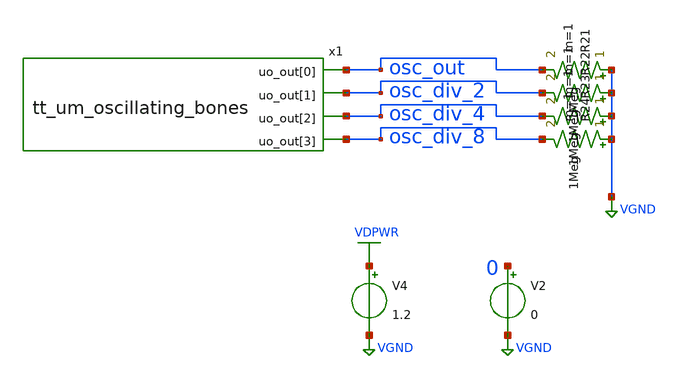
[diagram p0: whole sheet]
** sch_path: xschem/testbench.sch
**.subckt testbench
x1 osc_out osc_div_2 osc_div_4 osc_div_8 tt_um_oscillating_bones
R21 VGND osc_out 1Meg m=1
R22 VGND osc_div_2 1Meg m=1
R23 VGND osc_div_4 1Meg m=1
R24 VGND osc_div_8 1Meg m=1
V2 0 VGND 0
V4 VDPWR VGND 1.2
**** begin user architecture code

.lib $::SG13G2_MODELS/cornerMOSlv.lib mos_tt
.include ${PDK_ROOT}/${PDK}/libs.ref/sg13g2_stdcell/spice/sg13g2_stdcell.spice



.param temp=27
.param mc_ok=1

.tran 50p 200n
.save all

.control
run

meas tran tdiff TRIG osc_out VAL=1.1 RISE=2 TARG osc_out VAL=1.1 RISE=3
let osc_freq_mhz = (1 / (tdiff) / 1e6)
save osc_freq_mhz

meas tran tdiff_div2 TRIG osc_div_2 VAL=1.1 RISE=2 TARG osc_div_2 VAL=1.1 RISE=3
let osc_div_2_freq_mhz = (1 / (tdiff_div2) / 1e6)
save osc_div_2_freq_mhz

meas tran tdiff_div4 TRIG osc_div_4 VAL=1.1 RISE=2 TARG osc_div_4 VAL=1.1 RISE=3
let osc_div_4_freq_mhz = (1 / (tdiff_div4) / 1e6)
save osc_div_4_freq_mhz

meas tran tdiff_div8 TRIG osc_div_8 VAL=1.1 RISE=2 TARG osc_div_8 VAL=1.1 RISE=3
let osc_div_8_freq_mhz = (1 / (tdiff_div8) / 1e6)
save osc_div_8_freq_mhz

write testbench.raw
.endc


**** end user architecture code
**.ends

* expanding   symbol:  tt_um_oscillating_bones.sym # of pins=4
** sym_path: xschem/tt_um_oscillating_bones.sym
** sch_path: xschem/tt_um_oscillating_bones.sch
.subckt tt_um_oscillating_bones uo_out[0] uo_out[1] uo_out[2] uo_out[3]
*.opin uo_out[1]
*.opin uo_out[0]
*.opin uo_out[2]
*.opin uo_out[3]
x22 uo_out[1] uo_out[2] uo_out[3] uo_out[0] freq_divider
x1 uo_out[0] ring
.ends


* expanding   symbol:  freq_divider.sym # of pins=4
** sym_path: xschem/freq_divider.sym
** sch_path: xschem/freq_divider.sch
.subckt freq_divider ODIV2 ODIV4 ODIV8 IN
*.ipin IN
*.opin ODIV2
*.opin ODIV4
*.opin ODIV8
x4 ODIV2 net3 IN net3 VDPWR VDD VSS sg13g2_dfrbp_2
x1 ODIV4 net1 ODIV2 net1 VDPWR VDD VSS sg13g2_dfrbp_2
x2 ODIV8 net2 ODIV4 net2 VDPWR VDD VSS sg13g2_dfrbp_2
.ends


* expanding   symbol:  ring.sym # of pins=1
** sym_path: xschem/ring.sym
** sch_path: xschem/ring.sch
.subckt ring ROSC_OUT
*.opin ROSC_OUT
x1 net20 net1 skullfet_inverter
x2 net1 net3 skullfet_inverter
x3 net3 net2 skullfet_inverter
x4 net2 ROSC_OUT skullfet_inverter
x5 ROSC_OUT net4 skullfet_inverter
x7 net5 net6 skullfet_inverter
x6 net4 net5 skullfet_inverter
x8 net6 net7 skullfet_inverter
x9 net7 net11 skullfet_inverter
x10 net11 net8 skullfet_inverter
x11 net8 net9 skullfet_inverter
x12 net9 net10 skullfet_inverter
x13 net10 net12 skullfet_inverter
x14 net12 net13 skullfet_inverter
x15 net13 net14 skullfet_inverter
x16 net14 net15 skullfet_inverter
x17 net15 net16 skullfet_inverter
x18 net16 net17 skullfet_inverter
x19 net17 net18 skullfet_inverter
x20 net18 net19 skullfet_inverter
x21 net19 net20 skullfet_inverter
**** begin user architecture code


* Set an initial condition on net1 (0.0001 V) to break symmetry and assist DC operating point
*+ convergence in ngspice
.ic V(net1)=0.0001


**** end user architecture code
.ends


* expanding   symbol:  sg13g2_stdcells/sg13g2_dfrbp_2.sym # of pins=5
** sym_path: sg13g2_stdcells/sg13g2_dfrbp_2.sym
** sch_path: sg13g2_stdcells/sg13g2_dfrbp_2.sch
.subckt sg13g2_dfrbp_2 Q Q_N CLK D RESET_B VDD VSS
*.ipin D
*.ipin RESET_B
*.ipin CLK
*.opin Q
*.opin Q_N
*.iopin VDD
*.iopin VSS
XM1 Db D net12 VSS sg13_lv_nmos w=420.00n l=130.00n ng=1 m=1 mm_ok=1
XM2 net12 RESET_B VSS VSS sg13_lv_nmos w=420.00n l=130.00n ng=1 m=1 mm_ok=1
XM3 net2 clkneg net11 VSS sg13_lv_nmos w=420.00n l=130.00n ng=1 m=1 mm_ok=1
XM4 net11 net3 VSS VSS sg13_lv_nmos w=420.00n l=130.00n ng=1 m=1 mm_ok=1
XM5 net3 net2 net7 VSS sg13_lv_nmos w=420.00n l=130.00n ng=1 m=1 mm_ok=1
XM6 net7 RESET_B VSS VSS sg13_lv_nmos w=420.00n l=130.00n ng=1 m=1 mm_ok=1
XM7 Q_N net2 VSS VSS sg13_lv_nmos w=1.48u l=130.00n ng=2 m=1 mm_ok=1
XM8 net1 net2 VSS VSS sg13_lv_nmos w=640.00n l=130.00n ng=1 m=1 mm_ok=1
XM9 Q net1 VSS VSS sg13_lv_nmos w=1.48u l=130.00n ng=2 m=1 mm_ok=1
XM10 clkneg CLK VSS VSS sg13_lv_nmos w=740.00n l=130.00n ng=1 m=1 mm_ok=1
XM11 clkpos clkneg VSS VSS sg13_lv_nmos w=740.00n l=130.00n ng=1 m=1 mm_ok=1
XM12 Db clkneg net4 VSS sg13_lv_nmos w=420.00n l=130.00n ng=1 m=1 mm_ok=1
XM13 net4 clkpos net10 VSS sg13_lv_nmos w=420.00n l=130.00n ng=1 m=1 mm_ok=1
XM14 net10 net5 net6 VSS sg13_lv_nmos w=420.00n l=130.00n ng=1 m=1 mm_ok=1
XM15 net6 RESET_B VSS VSS sg13_lv_nmos w=420.00n l=130.00n ng=1 m=1 mm_ok=1
XM16 net5 net4 VSS VSS sg13_lv_nmos w=740.00n l=130.00n ng=1 m=1 mm_ok=1
XM17 net5 clkpos net2 VSS sg13_lv_nmos w=740.00n l=130.00n ng=1 m=1 mm_ok=1
XM18 Db RESET_B VDD VDD sg13_lv_pmos w=420.00n l=130.00n ng=1 m=1 mm_ok=1
XM19 Db D VDD VDD sg13_lv_pmos w=420.00n l=130.00n ng=1 m=1 mm_ok=1
XM20 net9 net3 VDD VDD sg13_lv_pmos w=420.00n l=130.00n ng=1 m=1 mm_ok=1
XM21 net2 clkpos net9 VDD sg13_lv_pmos w=420.00n l=130.00n ng=1 m=1 mm_ok=1
XM22 net3 net2 VDD VDD sg13_lv_pmos w=420.00n l=130.00n ng=1 m=1 mm_ok=1
XM23 net3 RESET_B VDD VDD sg13_lv_pmos w=420.00n l=130.00n ng=1 m=1 mm_ok=1
XM24 Q_N net2 VDD VDD sg13_lv_pmos w=2.24u l=130.00n ng=2 m=1 mm_ok=1
XM25 net1 net2 VDD VDD sg13_lv_pmos w=1.000u l=130.00n ng=1 m=1 mm_ok=1
XM26 Q net1 VDD VDD sg13_lv_pmos w=2.24u l=130.00n ng=2 m=1 mm_ok=1
XM27 clkneg CLK VDD VDD sg13_lv_pmos w=1.12u l=130.00n ng=1 m=1 mm_ok=1
XM28 clkpos clkneg VDD VDD sg13_lv_pmos w=1.12u l=130.00n ng=1 m=1 mm_ok=1
XM29 Db clkpos net4 VDD sg13_lv_pmos w=420.00n l=130.00n ng=1 m=1 mm_ok=1
XM30 net8 net5 VDD VDD sg13_lv_pmos w=420.00n l=130.00n ng=1 m=1 mm_ok=1
XM31 net4 clkneg net8 VDD sg13_lv_pmos w=420.00n l=130.00n ng=1 m=1 mm_ok=1
XM32 net4 RESET_B VDD VDD sg13_lv_pmos w=420.00n l=130.00n ng=1 m=1 mm_ok=1
XM33 net5 net4 VDD VDD sg13_lv_pmos w=1.000u l=130.00n ng=1 m=1 mm_ok=1
XM34 net5 clkneg net2 VDD sg13_lv_pmos w=1.000u l=130.00n ng=1 m=1 mm_ok=1
.ends


* expanding   symbol:  skullfet_inverter.sym # of pins=2
** sym_path: xschem/skullfet_inverter.sym
** sch_path: xschem/skullfet_inverter.sch
.subckt skullfet_inverter A Y
*.ipin A
*.opin Y
XM1 Y A VDPWR VDPWR sg13_lv_pmos w=0.15u l=0.13u ng=1 m=1 mm_ok=1
XM2 Y A VGND VGND sg13_lv_nmos w=0.15u l=0.13u ng=1 m=1 mm_ok=1
.ends

.GLOBAL VGND
.GLOBAL VDPWR
.end
